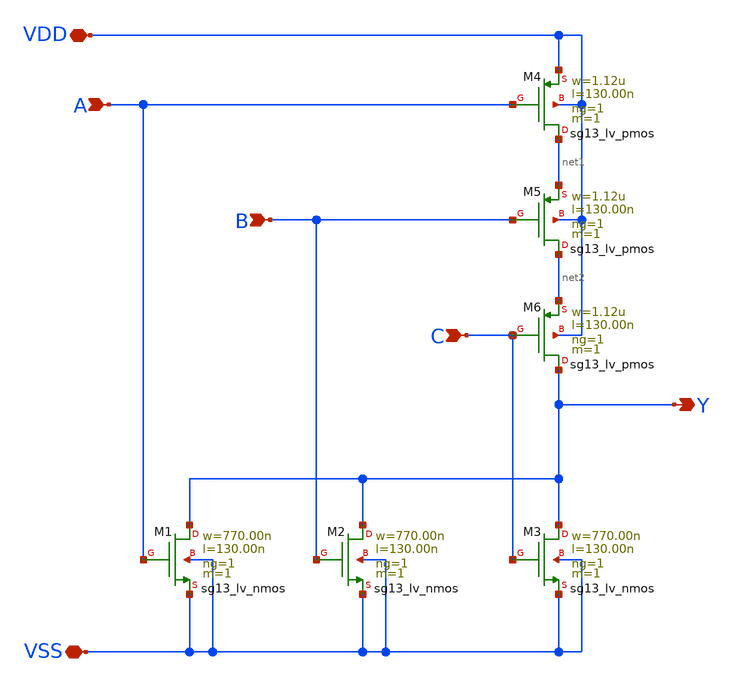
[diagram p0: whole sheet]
** sch_path: ihp-sg13g2/libs.tech/xschem/sg13g2_stdcells/sg13g2_nor3_1.sch
* Copyright 2023 IHP PDK Authors
* Licensed under the Apache License, Version 2.0 (the "License");
* you may not use this file except in compliance with the License.
* You may obtain a copy of the License at
* https://www.apache.org/licenses/LICENSE-2.0
* Unless required by applicable law or agreed to in writing, software
* distributed under the License is distributed on an "AS IS" BASIS,
* WITHOUT WARRANTIES OR CONDITIONS OF ANY KIND, either express or implied.
* See the License for the specific language governing permissions and
* limitations under the License.
**.subckt sg13g2_nor3_1 B VDD VSS Y A C
*.ipin B
*.iopin VDD
*.iopin VSS
*.opin Y
*.ipin A
*.ipin C
XM1 Y A VSS VSS sg13_lv_nmos w=770.00n l=130.00n ng=1 m=1 mm_ok=1
XM2 Y B VSS VSS sg13_lv_nmos w=770.00n l=130.00n ng=1 m=1 mm_ok=1
XM3 Y C VSS VSS sg13_lv_nmos w=770.00n l=130.00n ng=1 m=1 mm_ok=1
XM4 net1 A VDD VDD sg13_lv_pmos w=1.12u l=130.00n ng=1 m=1 mm_ok=1
XM5 net2 B net1 VDD sg13_lv_pmos w=1.12u l=130.00n ng=1 m=1 mm_ok=1
XM6 Y C net2 VDD sg13_lv_pmos w=1.12u l=130.00n ng=1 m=1 mm_ok=1
**.ends
.end
